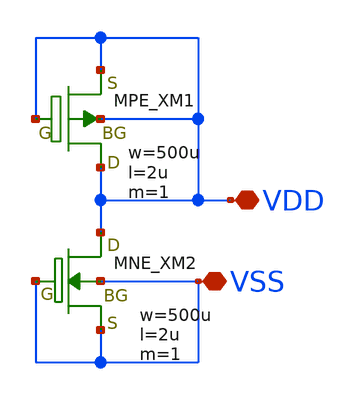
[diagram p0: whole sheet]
** sch_path: libs.tech/xschem/TR-1um_frame/OSS_ESD_5V_VDD.sch
**.subckt OSS_ESD_5V_VDD VDD VSS
*.iopin VDD
*.iopin VSS
XXM1 VDD VDD VDD VDD MPE w=500u l=2u as=0 ad=0 ps=0 pd=0 nrd=0 nrs=0 m=1
XXM2 VDD VSS VSS VSS MNE w=500u l=2u as=0 ad=0 ps=0 pd=0 nrd=0 nrs=0 m=1
**.ends
.end
